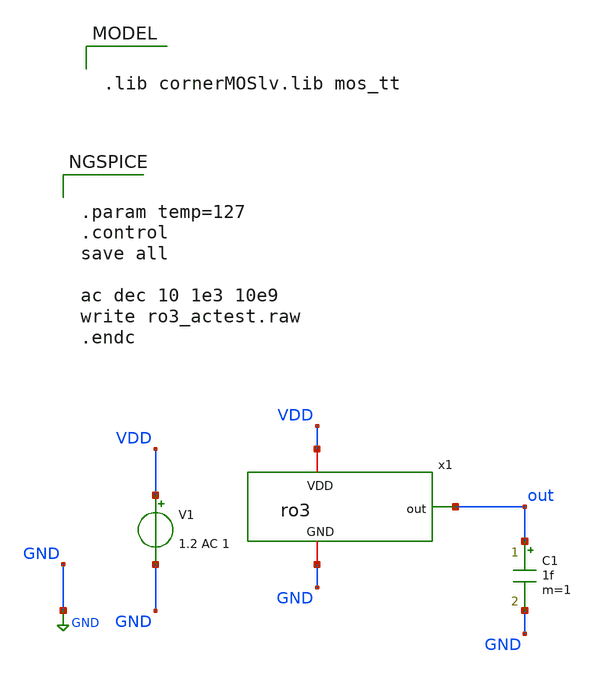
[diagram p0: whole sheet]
** sch_path: 20260718_ring_oscillator/ro3_tb_actest.sch
**.subckt ro3_tb_actest
x1 out VDD GND ro3
V1 VDD GND 1.2 AC 1
C1 out GND 1f m=1
**** begin user architecture code

.lib cornerMOSlv.lib mos_tt



.param temp=127
.control
save all

ac dec 10 1e3 10e9
write ro3_actest.raw
.endc


**** end user architecture code
**.ends

* expanding   symbol:  ro3.sym # of pins=3
** sym_path: 20260719_tunnable_ring_oscillator/ro3.sym
** sch_path: 20260719_tunnable_ring_oscillator/ro3.sch
.subckt ro3 out VDD GND
*.opin out
*.iopin VDD
*.iopin GND
XM1 net1 net2 GND GND sg13_lv_nmos w=0.15u l=0.13u ng=1 m=1 mm_ok=1
XM2 net1 net2 VDD VDD sg13_lv_pmos w=0.3u l=0.13u ng=1 m=1 mm_ok=1
XM3 net3 net1 GND GND sg13_lv_nmos w=0.15u l=0.13u ng=1 m=1 mm_ok=1
XM4 net3 net1 VDD VDD sg13_lv_pmos w=0.3u l=0.13u ng=1 m=1 mm_ok=1
XM5 net2 net3 GND GND sg13_lv_nmos w=0.15u l=0.13u ng=1 m=1 mm_ok=1
XM6 net2 net3 VDD VDD sg13_lv_pmos w=0.3u l=0.13u ng=1 m=1 mm_ok=1
XM7 out net2 GND GND sg13_lv_nmos w=0.15u l=0.13u ng=1 m=1 mm_ok=1
XM8 out net2 VDD VDD sg13_lv_pmos w=0.3u l=0.13u ng=1 m=1 mm_ok=1
.ends

.GLOBAL GND
.end
